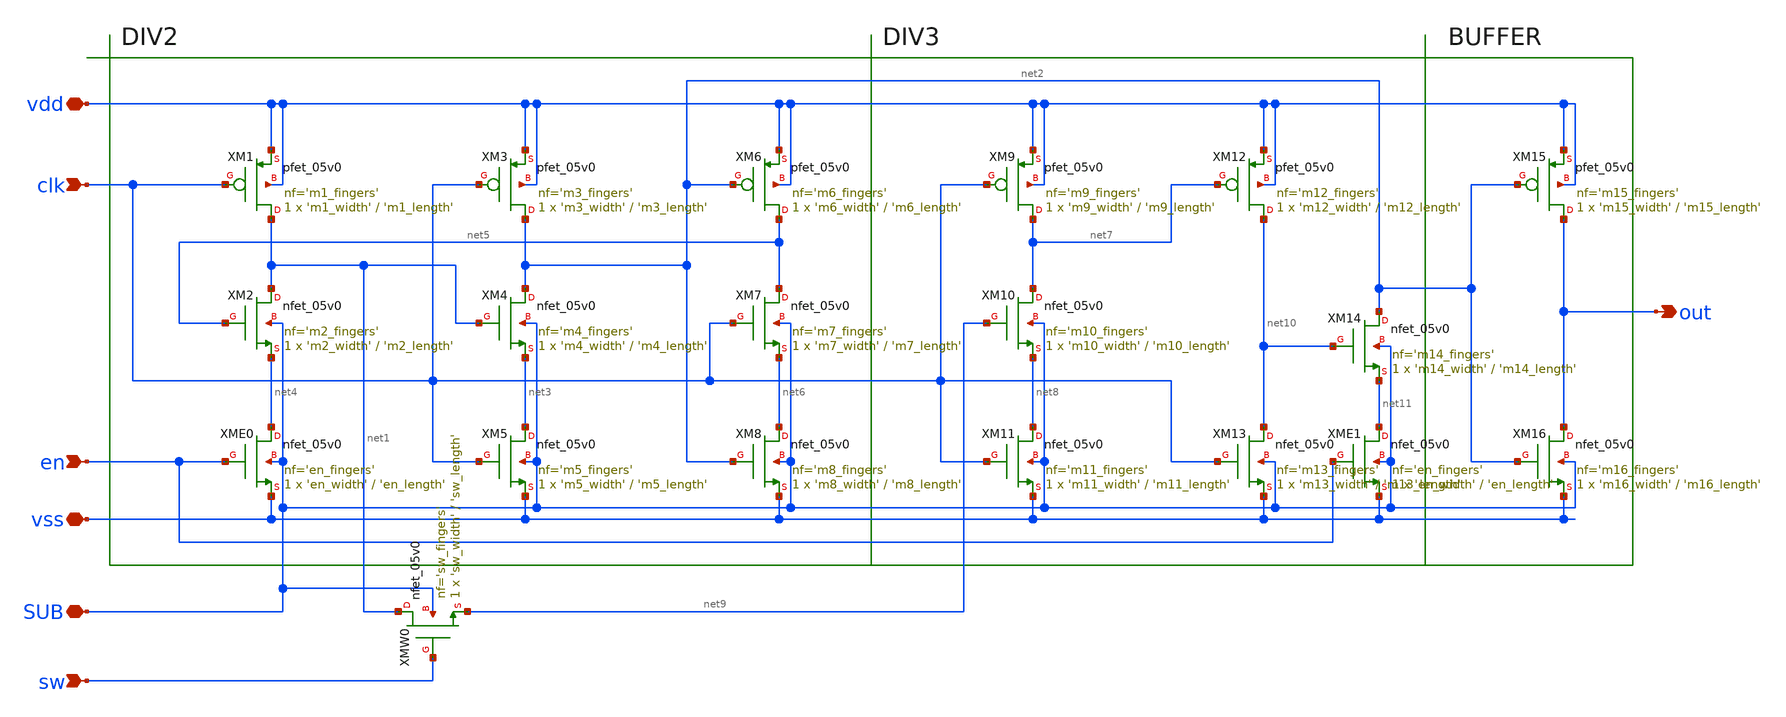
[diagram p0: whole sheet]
** sch_path: sch/divider/etspc_d2d3.sch
**.subckt etspc_d2d3 vss vdd clk sw en out SUB
*.iopin vss
*.iopin vdd
*.ipin clk
*.ipin sw
*.ipin en
*.opin out
*.iopin SUB
XM2 net1 net5 net4 SUB nfet_05v0 L='m2_length' W='m2_width' nf='m2_fingers' ad='int((nf+1)/2) * W/nf * 0.18u'
+ as='int((nf+2)/2) * W/nf * 0.18u' pd='2*int((nf+1)/2) * (W/nf + 0.18u)' ps='2*int((nf+2)/2) * (W/nf + 0.18u)'
+ nrd='0.18u / W' nrs='0.18u / W' sa=0 sb=0 sd=0 m=1
XM1 net1 clk vdd vdd pfet_05v0 L='m1_length' W='m1_width' nf='m1_fingers' ad='int((nf+1)/2) * W/nf * 0.18u'
+ as='int((nf+2)/2) * W/nf * 0.18u' pd='2*int((nf+1)/2) * (W/nf + 0.18u)' ps='2*int((nf+2)/2) * (W/nf + 0.18u)'
+ nrd='0.18u / W' nrs='0.18u / W' sa=0 sb=0 sd=0 m=1
XM3 net2 clk vdd vdd pfet_05v0 L='m3_length' W='m3_width' nf='m3_fingers' ad='int((nf+1)/2) * W/nf * 0.18u'
+ as='int((nf+2)/2) * W/nf * 0.18u' pd='2*int((nf+1)/2) * (W/nf + 0.18u)' ps='2*int((nf+2)/2) * (W/nf + 0.18u)'
+ nrd='0.18u / W' nrs='0.18u / W' sa=0 sb=0 sd=0 m=1
XM4 net2 net1 net3 SUB nfet_05v0 L='m4_length' W='m4_width' nf='m4_fingers' ad='int((nf+1)/2) * W/nf * 0.18u'
+ as='int((nf+2)/2) * W/nf * 0.18u' pd='2*int((nf+1)/2) * (W/nf + 0.18u)' ps='2*int((nf+2)/2) * (W/nf + 0.18u)'
+ nrd='0.18u / W' nrs='0.18u / W' sa=0 sb=0 sd=0 m=1
XM5 net3 clk vss SUB nfet_05v0 L='m5_length' W='m5_width' nf='m5_fingers' ad='int((nf+1)/2) * W/nf * 0.18u'
+ as='int((nf+2)/2) * W/nf * 0.18u' pd='2*int((nf+1)/2) * (W/nf + 0.18u)' ps='2*int((nf+2)/2) * (W/nf + 0.18u)'
+ nrd='0.18u / W' nrs='0.18u / W' sa=0 sb=0 sd=0 m=1
XM6 net5 net2 vdd vdd pfet_05v0 L='m6_length' W='m6_width' nf='m6_fingers' ad='int((nf+1)/2) * W/nf * 0.18u'
+ as='int((nf+2)/2) * W/nf * 0.18u' pd='2*int((nf+1)/2) * (W/nf + 0.18u)' ps='2*int((nf+2)/2) * (W/nf + 0.18u)'
+ nrd='0.18u / W' nrs='0.18u / W' sa=0 sb=0 sd=0 m=1
XM7 net5 clk net6 SUB nfet_05v0 L='m7_length' W='m7_width' nf='m7_fingers' ad='int((nf+1)/2) * W/nf * 0.18u'
+ as='int((nf+2)/2) * W/nf * 0.18u' pd='2*int((nf+1)/2) * (W/nf + 0.18u)' ps='2*int((nf+2)/2) * (W/nf + 0.18u)'
+ nrd='0.18u / W' nrs='0.18u / W' sa=0 sb=0 sd=0 m=1
XM8 net6 net2 vss SUB nfet_05v0 L='m8_length' W='m8_width' nf='m8_fingers' ad='int((nf+1)/2) * W/nf * 0.18u'
+ as='int((nf+2)/2) * W/nf * 0.18u' pd='2*int((nf+1)/2) * (W/nf + 0.18u)' ps='2*int((nf+2)/2) * (W/nf + 0.18u)'
+ nrd='0.18u / W' nrs='0.18u / W' sa=0 sb=0 sd=0 m=1
XME0 net4 en vss SUB nfet_05v0 L='en_length' W='en_width' nf='en_fingers' ad='int((nf+1)/2) * W/nf * 0.18u'
+ as='int((nf+2)/2) * W/nf * 0.18u' pd='2*int((nf+1)/2) * (W/nf + 0.18u)' ps='2*int((nf+2)/2) * (W/nf + 0.18u)'
+ nrd='0.18u / W' nrs='0.18u / W' sa=0 sb=0 sd=0 m=1
XMW0 net1 sw net9 SUB nfet_05v0 L='sw_length' W='sw_width' nf='sw_fingers' ad='int((nf+1)/2) * W/nf * 0.18u'
+ as='int((nf+2)/2) * W/nf * 0.18u' pd='2*int((nf+1)/2) * (W/nf + 0.18u)' ps='2*int((nf+2)/2) * (W/nf + 0.18u)'
+ nrd='0.18u / W' nrs='0.18u / W' sa=0 sb=0 sd=0 m=1
XM9 net7 clk vdd vdd pfet_05v0 L='m9_length' W='m9_width' nf='m9_fingers' ad='int((nf+1)/2) * W/nf * 0.18u'
+ as='int((nf+2)/2) * W/nf * 0.18u' pd='2*int((nf+1)/2) * (W/nf + 0.18u)' ps='2*int((nf+2)/2) * (W/nf + 0.18u)'
+ nrd='0.18u / W' nrs='0.18u / W' sa=0 sb=0 sd=0 m=1
XM10 net7 net9 net8 SUB nfet_05v0 L='m10_length' W='m10_width' nf='m10_fingers' ad='int((nf+1)/2) * W/nf * 0.18u'
+ as='int((nf+2)/2) * W/nf * 0.18u' pd='2*int((nf+1)/2) * (W/nf + 0.18u)' ps='2*int((nf+2)/2) * (W/nf + 0.18u)'
+ nrd='0.18u / W' nrs='0.18u / W' sa=0 sb=0 sd=0 m=1
XM11 net8 clk vss SUB nfet_05v0 L='m11_length' W='m11_width' nf='m11_fingers' ad='int((nf+1)/2) * W/nf * 0.18u'
+ as='int((nf+2)/2) * W/nf * 0.18u' pd='2*int((nf+1)/2) * (W/nf + 0.18u)' ps='2*int((nf+2)/2) * (W/nf + 0.18u)'
+ nrd='0.18u / W' nrs='0.18u / W' sa=0 sb=0 sd=0 m=1
XM12 net10 net7 vdd vdd pfet_05v0 L='m12_length' W='m12_width' nf='m12_fingers' ad='int((nf+1)/2) * W/nf * 0.18u'
+ as='int((nf+2)/2) * W/nf * 0.18u' pd='2*int((nf+1)/2) * (W/nf + 0.18u)' ps='2*int((nf+2)/2) * (W/nf + 0.18u)'
+ nrd='0.18u / W' nrs='0.18u / W' sa=0 sb=0 sd=0 m=1
XM13 net10 clk vss SUB nfet_05v0 L='m13_length' W='m13_width' nf='m13_fingers' ad='int((nf+1)/2) * W/nf * 0.18u'
+ as='int((nf+2)/2) * W/nf * 0.18u' pd='2*int((nf+1)/2) * (W/nf + 0.18u)' ps='2*int((nf+2)/2) * (W/nf + 0.18u)'
+ nrd='0.18u / W' nrs='0.18u / W' sa=0 sb=0 sd=0 m=1
XM14 net2 net10 net11 SUB nfet_05v0 L='m14_length' W='m14_width' nf='m14_fingers' ad='int((nf+1)/2) * W/nf * 0.18u'
+ as='int((nf+2)/2) * W/nf * 0.18u' pd='2*int((nf+1)/2) * (W/nf + 0.18u)' ps='2*int((nf+2)/2) * (W/nf + 0.18u)'
+ nrd='0.18u / W' nrs='0.18u / W' sa=0 sb=0 sd=0 m=1
XM15 out net2 vdd vdd pfet_05v0 L='m15_length' W='m15_width' nf='m15_fingers' ad='int((nf+1)/2) * W/nf * 0.18u'
+ as='int((nf+2)/2) * W/nf * 0.18u' pd='2*int((nf+1)/2) * (W/nf + 0.18u)' ps='2*int((nf+2)/2) * (W/nf + 0.18u)'
+ nrd='0.18u / W' nrs='0.18u / W' sa=0 sb=0 sd=0 m=1
XM16 out net2 vss SUB nfet_05v0 L='m16_length' W='m16_width' nf='m16_fingers' ad='int((nf+1)/2) * W/nf * 0.18u'
+ as='int((nf+2)/2) * W/nf * 0.18u' pd='2*int((nf+1)/2) * (W/nf + 0.18u)' ps='2*int((nf+2)/2) * (W/nf + 0.18u)'
+ nrd='0.18u / W' nrs='0.18u / W' sa=0 sb=0 sd=0 m=1
XME1 net11 en vss SUB nfet_05v0 L='en_length' W='en_width' nf='en_fingers' ad='int((nf+1)/2) * W/nf * 0.18u'
+ as='int((nf+2)/2) * W/nf * 0.18u' pd='2*int((nf+1)/2) * (W/nf + 0.18u)' ps='2*int((nf+2)/2) * (W/nf + 0.18u)'
+ nrd='0.18u / W' nrs='0.18u / W' sa=0 sb=0 sd=0 m=1
**.ends
.end
